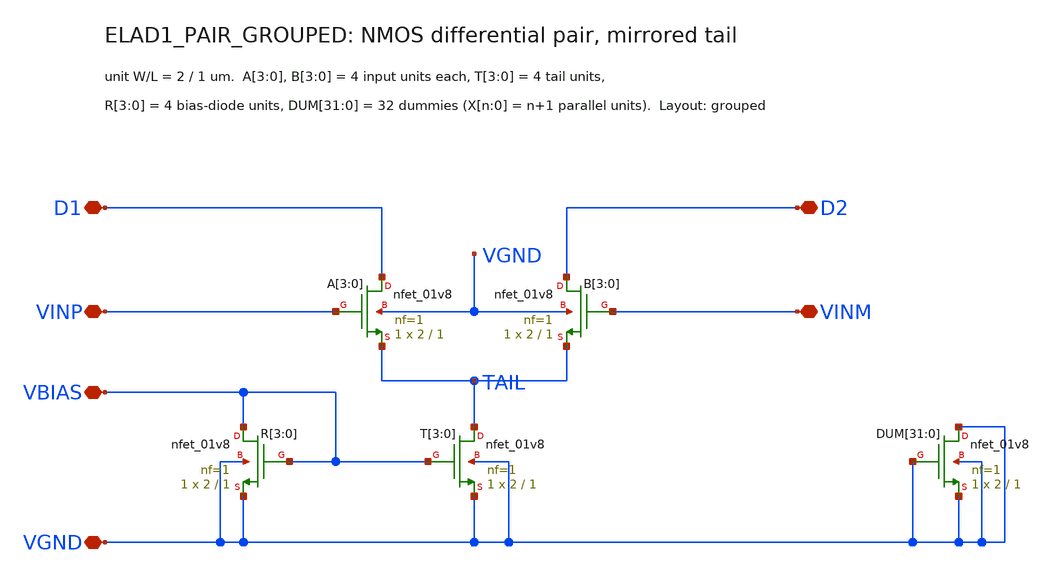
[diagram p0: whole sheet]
** sch_path: cells/ELAD1_PAIR_GROUPED/schematic/ELAD1_PAIR_GROUPED.sch
**.subckt ELAD1_PAIR_GROUPED D1 D2 VINP VINM VBIAS VGND
*.iopin D1
*.iopin D2
*.iopin VINP
*.iopin VINM
*.iopin VBIAS
*.iopin VGND
XA[3] D1 VINP TAIL VGND sky130_fd_pr__nfet_01v8 L=1 W=2 nf=1 ad='int((1 + 1)/2) * 2 / 1 * 0.29' as='int((1 + 2)/2) * 2 / 1 * 0.29'
+ pd='2*int((1 + 1)/2) * (2 / 1 + 0.29)' ps='2*int((1 + 2)/2) * (2 / 1 + 0.29)' nrd='0.29 / 2 ' nrs='0.29 / 2 '
+ sa=0 sb=0 sd=0 mult=1 m=1
XA[2] D1 VINP TAIL VGND sky130_fd_pr__nfet_01v8 L=1 W=2 nf=1 ad='int((1 + 1)/2) * 2 / 1 * 0.29' as='int((1 + 2)/2) * 2 / 1 * 0.29'
+ pd='2*int((1 + 1)/2) * (2 / 1 + 0.29)' ps='2*int((1 + 2)/2) * (2 / 1 + 0.29)' nrd='0.29 / 2 ' nrs='0.29 / 2 '
+ sa=0 sb=0 sd=0 mult=1 m=1
XA[1] D1 VINP TAIL VGND sky130_fd_pr__nfet_01v8 L=1 W=2 nf=1 ad='int((1 + 1)/2) * 2 / 1 * 0.29' as='int((1 + 2)/2) * 2 / 1 * 0.29'
+ pd='2*int((1 + 1)/2) * (2 / 1 + 0.29)' ps='2*int((1 + 2)/2) * (2 / 1 + 0.29)' nrd='0.29 / 2 ' nrs='0.29 / 2 '
+ sa=0 sb=0 sd=0 mult=1 m=1
XA[0] D1 VINP TAIL VGND sky130_fd_pr__nfet_01v8 L=1 W=2 nf=1 ad='int((1 + 1)/2) * 2 / 1 * 0.29' as='int((1 + 2)/2) * 2 / 1 * 0.29'
+ pd='2*int((1 + 1)/2) * (2 / 1 + 0.29)' ps='2*int((1 + 2)/2) * (2 / 1 + 0.29)' nrd='0.29 / 2 ' nrs='0.29 / 2 '
+ sa=0 sb=0 sd=0 mult=1 m=1
XB[3] D2 VINM TAIL VGND sky130_fd_pr__nfet_01v8 L=1 W=2 nf=1 ad='int((1 + 1)/2) * 2 / 1 * 0.29' as='int((1 + 2)/2) * 2 / 1 * 0.29'
+ pd='2*int((1 + 1)/2) * (2 / 1 + 0.29)' ps='2*int((1 + 2)/2) * (2 / 1 + 0.29)' nrd='0.29 / 2 ' nrs='0.29 / 2 '
+ sa=0 sb=0 sd=0 mult=1 m=1
XB[2] D2 VINM TAIL VGND sky130_fd_pr__nfet_01v8 L=1 W=2 nf=1 ad='int((1 + 1)/2) * 2 / 1 * 0.29' as='int((1 + 2)/2) * 2 / 1 * 0.29'
+ pd='2*int((1 + 1)/2) * (2 / 1 + 0.29)' ps='2*int((1 + 2)/2) * (2 / 1 + 0.29)' nrd='0.29 / 2 ' nrs='0.29 / 2 '
+ sa=0 sb=0 sd=0 mult=1 m=1
XB[1] D2 VINM TAIL VGND sky130_fd_pr__nfet_01v8 L=1 W=2 nf=1 ad='int((1 + 1)/2) * 2 / 1 * 0.29' as='int((1 + 2)/2) * 2 / 1 * 0.29'
+ pd='2*int((1 + 1)/2) * (2 / 1 + 0.29)' ps='2*int((1 + 2)/2) * (2 / 1 + 0.29)' nrd='0.29 / 2 ' nrs='0.29 / 2 '
+ sa=0 sb=0 sd=0 mult=1 m=1
XB[0] D2 VINM TAIL VGND sky130_fd_pr__nfet_01v8 L=1 W=2 nf=1 ad='int((1 + 1)/2) * 2 / 1 * 0.29' as='int((1 + 2)/2) * 2 / 1 * 0.29'
+ pd='2*int((1 + 1)/2) * (2 / 1 + 0.29)' ps='2*int((1 + 2)/2) * (2 / 1 + 0.29)' nrd='0.29 / 2 ' nrs='0.29 / 2 '
+ sa=0 sb=0 sd=0 mult=1 m=1
XT[3] TAIL VBIAS VGND VGND sky130_fd_pr__nfet_01v8 L=1 W=2 nf=1 ad='int((1 + 1)/2) * 2 / 1 * 0.29' as='int((1 + 2)/2) * 2 / 1 * 0.29'
+ pd='2*int((1 + 1)/2) * (2 / 1 + 0.29)' ps='2*int((1 + 2)/2) * (2 / 1 + 0.29)' nrd='0.29 / 2 ' nrs='0.29 / 2 '
+ sa=0 sb=0 sd=0 mult=1 m=1
XT[2] TAIL VBIAS VGND VGND sky130_fd_pr__nfet_01v8 L=1 W=2 nf=1 ad='int((1 + 1)/2) * 2 / 1 * 0.29' as='int((1 + 2)/2) * 2 / 1 * 0.29'
+ pd='2*int((1 + 1)/2) * (2 / 1 + 0.29)' ps='2*int((1 + 2)/2) * (2 / 1 + 0.29)' nrd='0.29 / 2 ' nrs='0.29 / 2 '
+ sa=0 sb=0 sd=0 mult=1 m=1
XT[1] TAIL VBIAS VGND VGND sky130_fd_pr__nfet_01v8 L=1 W=2 nf=1 ad='int((1 + 1)/2) * 2 / 1 * 0.29' as='int((1 + 2)/2) * 2 / 1 * 0.29'
+ pd='2*int((1 + 1)/2) * (2 / 1 + 0.29)' ps='2*int((1 + 2)/2) * (2 / 1 + 0.29)' nrd='0.29 / 2 ' nrs='0.29 / 2 '
+ sa=0 sb=0 sd=0 mult=1 m=1
XT[0] TAIL VBIAS VGND VGND sky130_fd_pr__nfet_01v8 L=1 W=2 nf=1 ad='int((1 + 1)/2) * 2 / 1 * 0.29' as='int((1 + 2)/2) * 2 / 1 * 0.29'
+ pd='2*int((1 + 1)/2) * (2 / 1 + 0.29)' ps='2*int((1 + 2)/2) * (2 / 1 + 0.29)' nrd='0.29 / 2 ' nrs='0.29 / 2 '
+ sa=0 sb=0 sd=0 mult=1 m=1
XR[3] VBIAS VBIAS VGND VGND sky130_fd_pr__nfet_01v8 L=1 W=2 nf=1 ad='int((1 + 1)/2) * 2 / 1 * 0.29' as='int((1 + 2)/2) * 2 / 1 * 0.29'
+ pd='2*int((1 + 1)/2) * (2 / 1 + 0.29)' ps='2*int((1 + 2)/2) * (2 / 1 + 0.29)' nrd='0.29 / 2 ' nrs='0.29 / 2 '
+ sa=0 sb=0 sd=0 mult=1 m=1
XR[2] VBIAS VBIAS VGND VGND sky130_fd_pr__nfet_01v8 L=1 W=2 nf=1 ad='int((1 + 1)/2) * 2 / 1 * 0.29' as='int((1 + 2)/2) * 2 / 1 * 0.29'
+ pd='2*int((1 + 1)/2) * (2 / 1 + 0.29)' ps='2*int((1 + 2)/2) * (2 / 1 + 0.29)' nrd='0.29 / 2 ' nrs='0.29 / 2 '
+ sa=0 sb=0 sd=0 mult=1 m=1
XR[1] VBIAS VBIAS VGND VGND sky130_fd_pr__nfet_01v8 L=1 W=2 nf=1 ad='int((1 + 1)/2) * 2 / 1 * 0.29' as='int((1 + 2)/2) * 2 / 1 * 0.29'
+ pd='2*int((1 + 1)/2) * (2 / 1 + 0.29)' ps='2*int((1 + 2)/2) * (2 / 1 + 0.29)' nrd='0.29 / 2 ' nrs='0.29 / 2 '
+ sa=0 sb=0 sd=0 mult=1 m=1
XR[0] VBIAS VBIAS VGND VGND sky130_fd_pr__nfet_01v8 L=1 W=2 nf=1 ad='int((1 + 1)/2) * 2 / 1 * 0.29' as='int((1 + 2)/2) * 2 / 1 * 0.29'
+ pd='2*int((1 + 1)/2) * (2 / 1 + 0.29)' ps='2*int((1 + 2)/2) * (2 / 1 + 0.29)' nrd='0.29 / 2 ' nrs='0.29 / 2 '
+ sa=0 sb=0 sd=0 mult=1 m=1
XDUM[31] VGND VGND VGND VGND sky130_fd_pr__nfet_01v8 L=1 W=2 nf=1 ad='int((1 + 1)/2) * 2 / 1 * 0.29'
+ as='int((1 + 2)/2) * 2 / 1 * 0.29' pd='2*int((1 + 1)/2) * (2 / 1 + 0.29)' ps='2*int((1 + 2)/2) * (2 / 1 + 0.29)'
+ nrd='0.29 / 2 ' nrs='0.29 / 2 ' sa=0 sb=0 sd=0 mult=1 m=1
XDUM[30] VGND VGND VGND VGND sky130_fd_pr__nfet_01v8 L=1 W=2 nf=1 ad='int((1 + 1)/2) * 2 / 1 * 0.29'
+ as='int((1 + 2)/2) * 2 / 1 * 0.29' pd='2*int((1 + 1)/2) * (2 / 1 + 0.29)' ps='2*int((1 + 2)/2) * (2 / 1 + 0.29)'
+ nrd='0.29 / 2 ' nrs='0.29 / 2 ' sa=0 sb=0 sd=0 mult=1 m=1
XDUM[29] VGND VGND VGND VGND sky130_fd_pr__nfet_01v8 L=1 W=2 nf=1 ad='int((1 + 1)/2) * 2 / 1 * 0.29'
+ as='int((1 + 2)/2) * 2 / 1 * 0.29' pd='2*int((1 + 1)/2) * (2 / 1 + 0.29)' ps='2*int((1 + 2)/2) * (2 / 1 + 0.29)'
+ nrd='0.29 / 2 ' nrs='0.29 / 2 ' sa=0 sb=0 sd=0 mult=1 m=1
XDUM[28] VGND VGND VGND VGND sky130_fd_pr__nfet_01v8 L=1 W=2 nf=1 ad='int((1 + 1)/2) * 2 / 1 * 0.29'
+ as='int((1 + 2)/2) * 2 / 1 * 0.29' pd='2*int((1 + 1)/2) * (2 / 1 + 0.29)' ps='2*int((1 + 2)/2) * (2 / 1 + 0.29)'
+ nrd='0.29 / 2 ' nrs='0.29 / 2 ' sa=0 sb=0 sd=0 mult=1 m=1
XDUM[27] VGND VGND VGND VGND sky130_fd_pr__nfet_01v8 L=1 W=2 nf=1 ad='int((1 + 1)/2) * 2 / 1 * 0.29'
+ as='int((1 + 2)/2) * 2 / 1 * 0.29' pd='2*int((1 + 1)/2) * (2 / 1 + 0.29)' ps='2*int((1 + 2)/2) * (2 / 1 + 0.29)'
+ nrd='0.29 / 2 ' nrs='0.29 / 2 ' sa=0 sb=0 sd=0 mult=1 m=1
XDUM[26] VGND VGND VGND VGND sky130_fd_pr__nfet_01v8 L=1 W=2 nf=1 ad='int((1 + 1)/2) * 2 / 1 * 0.29'
+ as='int((1 + 2)/2) * 2 / 1 * 0.29' pd='2*int((1 + 1)/2) * (2 / 1 + 0.29)' ps='2*int((1 + 2)/2) * (2 / 1 + 0.29)'
+ nrd='0.29 / 2 ' nrs='0.29 / 2 ' sa=0 sb=0 sd=0 mult=1 m=1
XDUM[25] VGND VGND VGND VGND sky130_fd_pr__nfet_01v8 L=1 W=2 nf=1 ad='int((1 + 1)/2) * 2 / 1 * 0.29'
+ as='int((1 + 2)/2) * 2 / 1 * 0.29' pd='2*int((1 + 1)/2) * (2 / 1 + 0.29)' ps='2*int((1 + 2)/2) * (2 / 1 + 0.29)'
+ nrd='0.29 / 2 ' nrs='0.29 / 2 ' sa=0 sb=0 sd=0 mult=1 m=1
XDUM[24] VGND VGND VGND VGND sky130_fd_pr__nfet_01v8 L=1 W=2 nf=1 ad='int((1 + 1)/2) * 2 / 1 * 0.29'
+ as='int((1 + 2)/2) * 2 / 1 * 0.29' pd='2*int((1 + 1)/2) * (2 / 1 + 0.29)' ps='2*int((1 + 2)/2) * (2 / 1 + 0.29)'
+ nrd='0.29 / 2 ' nrs='0.29 / 2 ' sa=0 sb=0 sd=0 mult=1 m=1
XDUM[23] VGND VGND VGND VGND sky130_fd_pr__nfet_01v8 L=1 W=2 nf=1 ad='int((1 + 1)/2) * 2 / 1 * 0.29'
+ as='int((1 + 2)/2) * 2 / 1 * 0.29' pd='2*int((1 + 1)/2) * (2 / 1 + 0.29)' ps='2*int((1 + 2)/2) * (2 / 1 + 0.29)'
+ nrd='0.29 / 2 ' nrs='0.29 / 2 ' sa=0 sb=0 sd=0 mult=1 m=1
XDUM[22] VGND VGND VGND VGND sky130_fd_pr__nfet_01v8 L=1 W=2 nf=1 ad='int((1 + 1)/2) * 2 / 1 * 0.29'
+ as='int((1 + 2)/2) * 2 / 1 * 0.29' pd='2*int((1 + 1)/2) * (2 / 1 + 0.29)' ps='2*int((1 + 2)/2) * (2 / 1 + 0.29)'
+ nrd='0.29 / 2 ' nrs='0.29 / 2 ' sa=0 sb=0 sd=0 mult=1 m=1
XDUM[21] VGND VGND VGND VGND sky130_fd_pr__nfet_01v8 L=1 W=2 nf=1 ad='int((1 + 1)/2) * 2 / 1 * 0.29'
+ as='int((1 + 2)/2) * 2 / 1 * 0.29' pd='2*int((1 + 1)/2) * (2 / 1 + 0.29)' ps='2*int((1 + 2)/2) * (2 / 1 + 0.29)'
+ nrd='0.29 / 2 ' nrs='0.29 / 2 ' sa=0 sb=0 sd=0 mult=1 m=1
XDUM[20] VGND VGND VGND VGND sky130_fd_pr__nfet_01v8 L=1 W=2 nf=1 ad='int((1 + 1)/2) * 2 / 1 * 0.29'
+ as='int((1 + 2)/2) * 2 / 1 * 0.29' pd='2*int((1 + 1)/2) * (2 / 1 + 0.29)' ps='2*int((1 + 2)/2) * (2 / 1 + 0.29)'
+ nrd='0.29 / 2 ' nrs='0.29 / 2 ' sa=0 sb=0 sd=0 mult=1 m=1
XDUM[19] VGND VGND VGND VGND sky130_fd_pr__nfet_01v8 L=1 W=2 nf=1 ad='int((1 + 1)/2) * 2 / 1 * 0.29'
+ as='int((1 + 2)/2) * 2 / 1 * 0.29' pd='2*int((1 + 1)/2) * (2 / 1 + 0.29)' ps='2*int((1 + 2)/2) * (2 / 1 + 0.29)'
+ nrd='0.29 / 2 ' nrs='0.29 / 2 ' sa=0 sb=0 sd=0 mult=1 m=1
XDUM[18] VGND VGND VGND VGND sky130_fd_pr__nfet_01v8 L=1 W=2 nf=1 ad='int((1 + 1)/2) * 2 / 1 * 0.29'
+ as='int((1 + 2)/2) * 2 / 1 * 0.29' pd='2*int((1 + 1)/2) * (2 / 1 + 0.29)' ps='2*int((1 + 2)/2) * (2 / 1 + 0.29)'
+ nrd='0.29 / 2 ' nrs='0.29 / 2 ' sa=0 sb=0 sd=0 mult=1 m=1
XDUM[17] VGND VGND VGND VGND sky130_fd_pr__nfet_01v8 L=1 W=2 nf=1 ad='int((1 + 1)/2) * 2 / 1 * 0.29'
+ as='int((1 + 2)/2) * 2 / 1 * 0.29' pd='2*int((1 + 1)/2) * (2 / 1 + 0.29)' ps='2*int((1 + 2)/2) * (2 / 1 + 0.29)'
+ nrd='0.29 / 2 ' nrs='0.29 / 2 ' sa=0 sb=0 sd=0 mult=1 m=1
XDUM[16] VGND VGND VGND VGND sky130_fd_pr__nfet_01v8 L=1 W=2 nf=1 ad='int((1 + 1)/2) * 2 / 1 * 0.29'
+ as='int((1 + 2)/2) * 2 / 1 * 0.29' pd='2*int((1 + 1)/2) * (2 / 1 + 0.29)' ps='2*int((1 + 2)/2) * (2 / 1 + 0.29)'
+ nrd='0.29 / 2 ' nrs='0.29 / 2 ' sa=0 sb=0 sd=0 mult=1 m=1
XDUM[15] VGND VGND VGND VGND sky130_fd_pr__nfet_01v8 L=1 W=2 nf=1 ad='int((1 + 1)/2) * 2 / 1 * 0.29'
+ as='int((1 + 2)/2) * 2 / 1 * 0.29' pd='2*int((1 + 1)/2) * (2 / 1 + 0.29)' ps='2*int((1 + 2)/2) * (2 / 1 + 0.29)'
+ nrd='0.29 / 2 ' nrs='0.29 / 2 ' sa=0 sb=0 sd=0 mult=1 m=1
XDUM[14] VGND VGND VGND VGND sky130_fd_pr__nfet_01v8 L=1 W=2 nf=1 ad='int((1 + 1)/2) * 2 / 1 * 0.29'
+ as='int((1 + 2)/2) * 2 / 1 * 0.29' pd='2*int((1 + 1)/2) * (2 / 1 + 0.29)' ps='2*int((1 + 2)/2) * (2 / 1 + 0.29)'
+ nrd='0.29 / 2 ' nrs='0.29 / 2 ' sa=0 sb=0 sd=0 mult=1 m=1
XDUM[13] VGND VGND VGND VGND sky130_fd_pr__nfet_01v8 L=1 W=2 nf=1 ad='int((1 + 1)/2) * 2 / 1 * 0.29'
+ as='int((1 + 2)/2) * 2 / 1 * 0.29' pd='2*int((1 + 1)/2) * (2 / 1 + 0.29)' ps='2*int((1 + 2)/2) * (2 / 1 + 0.29)'
+ nrd='0.29 / 2 ' nrs='0.29 / 2 ' sa=0 sb=0 sd=0 mult=1 m=1
XDUM[12] VGND VGND VGND VGND sky130_fd_pr__nfet_01v8 L=1 W=2 nf=1 ad='int((1 + 1)/2) * 2 / 1 * 0.29'
+ as='int((1 + 2)/2) * 2 / 1 * 0.29' pd='2*int((1 + 1)/2) * (2 / 1 + 0.29)' ps='2*int((1 + 2)/2) * (2 / 1 + 0.29)'
+ nrd='0.29 / 2 ' nrs='0.29 / 2 ' sa=0 sb=0 sd=0 mult=1 m=1
XDUM[11] VGND VGND VGND VGND sky130_fd_pr__nfet_01v8 L=1 W=2 nf=1 ad='int((1 + 1)/2) * 2 / 1 * 0.29'
+ as='int((1 + 2)/2) * 2 / 1 * 0.29' pd='2*int((1 + 1)/2) * (2 / 1 + 0.29)' ps='2*int((1 + 2)/2) * (2 / 1 + 0.29)'
+ nrd='0.29 / 2 ' nrs='0.29 / 2 ' sa=0 sb=0 sd=0 mult=1 m=1
XDUM[10] VGND VGND VGND VGND sky130_fd_pr__nfet_01v8 L=1 W=2 nf=1 ad='int((1 + 1)/2) * 2 / 1 * 0.29'
+ as='int((1 + 2)/2) * 2 / 1 * 0.29' pd='2*int((1 + 1)/2) * (2 / 1 + 0.29)' ps='2*int((1 + 2)/2) * (2 / 1 + 0.29)'
+ nrd='0.29 / 2 ' nrs='0.29 / 2 ' sa=0 sb=0 sd=0 mult=1 m=1
XDUM[9] VGND VGND VGND VGND sky130_fd_pr__nfet_01v8 L=1 W=2 nf=1 ad='int((1 + 1)/2) * 2 / 1 * 0.29' as='int((1 + 2)/2) * 2 / 1 * 0.29'
+ pd='2*int((1 + 1)/2) * (2 / 1 + 0.29)' ps='2*int((1 + 2)/2) * (2 / 1 + 0.29)' nrd='0.29 / 2 ' nrs='0.29 / 2 '
+ sa=0 sb=0 sd=0 mult=1 m=1
XDUM[8] VGND VGND VGND VGND sky130_fd_pr__nfet_01v8 L=1 W=2 nf=1 ad='int((1 + 1)/2) * 2 / 1 * 0.29' as='int((1 + 2)/2) * 2 / 1 * 0.29'
+ pd='2*int((1 + 1)/2) * (2 / 1 + 0.29)' ps='2*int((1 + 2)/2) * (2 / 1 + 0.29)' nrd='0.29 / 2 ' nrs='0.29 / 2 '
+ sa=0 sb=0 sd=0 mult=1 m=1
XDUM[7] VGND VGND VGND VGND sky130_fd_pr__nfet_01v8 L=1 W=2 nf=1 ad='int((1 + 1)/2) * 2 / 1 * 0.29' as='int((1 + 2)/2) * 2 / 1 * 0.29'
+ pd='2*int((1 + 1)/2) * (2 / 1 + 0.29)' ps='2*int((1 + 2)/2) * (2 / 1 + 0.29)' nrd='0.29 / 2 ' nrs='0.29 / 2 '
+ sa=0 sb=0 sd=0 mult=1 m=1
XDUM[6] VGND VGND VGND VGND sky130_fd_pr__nfet_01v8 L=1 W=2 nf=1 ad='int((1 + 1)/2) * 2 / 1 * 0.29' as='int((1 + 2)/2) * 2 / 1 * 0.29'
+ pd='2*int((1 + 1)/2) * (2 / 1 + 0.29)' ps='2*int((1 + 2)/2) * (2 / 1 + 0.29)' nrd='0.29 / 2 ' nrs='0.29 / 2 '
+ sa=0 sb=0 sd=0 mult=1 m=1
XDUM[5] VGND VGND VGND VGND sky130_fd_pr__nfet_01v8 L=1 W=2 nf=1 ad='int((1 + 1)/2) * 2 / 1 * 0.29' as='int((1 + 2)/2) * 2 / 1 * 0.29'
+ pd='2*int((1 + 1)/2) * (2 / 1 + 0.29)' ps='2*int((1 + 2)/2) * (2 / 1 + 0.29)' nrd='0.29 / 2 ' nrs='0.29 / 2 '
+ sa=0 sb=0 sd=0 mult=1 m=1
XDUM[4] VGND VGND VGND VGND sky130_fd_pr__nfet_01v8 L=1 W=2 nf=1 ad='int((1 + 1)/2) * 2 / 1 * 0.29' as='int((1 + 2)/2) * 2 / 1 * 0.29'
+ pd='2*int((1 + 1)/2) * (2 / 1 + 0.29)' ps='2*int((1 + 2)/2) * (2 / 1 + 0.29)' nrd='0.29 / 2 ' nrs='0.29 / 2 '
+ sa=0 sb=0 sd=0 mult=1 m=1
XDUM[3] VGND VGND VGND VGND sky130_fd_pr__nfet_01v8 L=1 W=2 nf=1 ad='int((1 + 1)/2) * 2 / 1 * 0.29' as='int((1 + 2)/2) * 2 / 1 * 0.29'
+ pd='2*int((1 + 1)/2) * (2 / 1 + 0.29)' ps='2*int((1 + 2)/2) * (2 / 1 + 0.29)' nrd='0.29 / 2 ' nrs='0.29 / 2 '
+ sa=0 sb=0 sd=0 mult=1 m=1
XDUM[2] VGND VGND VGND VGND sky130_fd_pr__nfet_01v8 L=1 W=2 nf=1 ad='int((1 + 1)/2) * 2 / 1 * 0.29' as='int((1 + 2)/2) * 2 / 1 * 0.29'
+ pd='2*int((1 + 1)/2) * (2 / 1 + 0.29)' ps='2*int((1 + 2)/2) * (2 / 1 + 0.29)' nrd='0.29 / 2 ' nrs='0.29 / 2 '
+ sa=0 sb=0 sd=0 mult=1 m=1
XDUM[1] VGND VGND VGND VGND sky130_fd_pr__nfet_01v8 L=1 W=2 nf=1 ad='int((1 + 1)/2) * 2 / 1 * 0.29' as='int((1 + 2)/2) * 2 / 1 * 0.29'
+ pd='2*int((1 + 1)/2) * (2 / 1 + 0.29)' ps='2*int((1 + 2)/2) * (2 / 1 + 0.29)' nrd='0.29 / 2 ' nrs='0.29 / 2 '
+ sa=0 sb=0 sd=0 mult=1 m=1
XDUM[0] VGND VGND VGND VGND sky130_fd_pr__nfet_01v8 L=1 W=2 nf=1 ad='int((1 + 1)/2) * 2 / 1 * 0.29' as='int((1 + 2)/2) * 2 / 1 * 0.29'
+ pd='2*int((1 + 1)/2) * (2 / 1 + 0.29)' ps='2*int((1 + 2)/2) * (2 / 1 + 0.29)' nrd='0.29 / 2 ' nrs='0.29 / 2 '
+ sa=0 sb=0 sd=0 mult=1 m=1
**.ends
.end
